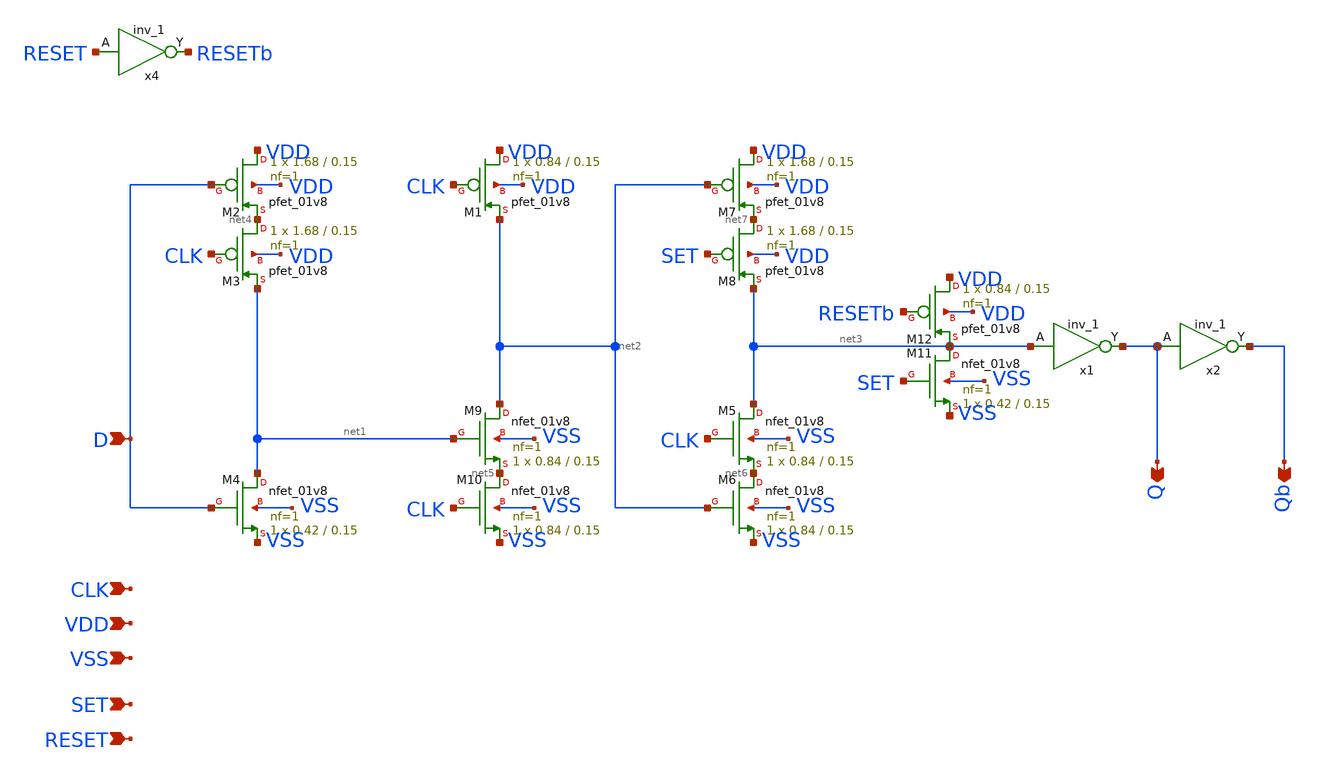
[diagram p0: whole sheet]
** sch_path: module/sample_clk_gen/dff_4.sch
**.subckt dff_4 D Q Qb CLK VDD VSS SET RESET
*.ipin D
*.opin Q
*.opin Qb
*.ipin CLK
*.ipin VDD
*.ipin VSS
*.ipin SET
*.ipin RESET
XM2 VDD D net4 VDD sky130_fd_pr__pfet_01v8 L=0.15 W=1.68 nf=1 ad='int((nf+1)/2) * W/nf * 0.29' as='int((nf+2)/2) * W/nf * 0.29'
+ pd='2*int((nf+1)/2) * (W/nf + 0.29)' ps='2*int((nf+2)/2) * (W/nf + 0.29)' nrd='0.29 / W' nrs='0.29 / W'
+ sa=0 sb=0 sd=0 mult=1 m=1
XM3 net4 CLK net1 VDD sky130_fd_pr__pfet_01v8 L=0.15 W=1.68 nf=1 ad='int((nf+1)/2) * W/nf * 0.29' as='int((nf+2)/2) * W/nf * 0.29'
+ pd='2*int((nf+1)/2) * (W/nf + 0.29)' ps='2*int((nf+2)/2) * (W/nf + 0.29)' nrd='0.29 / W' nrs='0.29 / W'
+ sa=0 sb=0 sd=0 mult=1 m=1
XM9 net2 net1 net5 VSS sky130_fd_pr__nfet_01v8 L=0.15 W=0.84 nf=1 ad='int((nf+1)/2) * W/nf * 0.29' as='int((nf+2)/2) * W/nf * 0.29'
+ pd='2*int((nf+1)/2) * (W/nf + 0.29)' ps='2*int((nf+2)/2) * (W/nf + 0.29)' nrd='0.29 / W' nrs='0.29 / W'
+ sa=0 sb=0 sd=0 mult=1 m=1
XM10 net5 CLK VSS VSS sky130_fd_pr__nfet_01v8 L=0.15 W=0.84 nf=1 ad='int((nf+1)/2) * W/nf * 0.29' as='int((nf+2)/2) * W/nf * 0.29'
+ pd='2*int((nf+1)/2) * (W/nf + 0.29)' ps='2*int((nf+2)/2) * (W/nf + 0.29)' nrd='0.29 / W' nrs='0.29 / W'
+ sa=0 sb=0 sd=0 mult=1 m=1
XM1 VDD CLK net2 VDD sky130_fd_pr__pfet_01v8 L=0.15 W=0.84 nf=1 ad='int((nf+1)/2) * W/nf * 0.29' as='int((nf+2)/2) * W/nf * 0.29'
+ pd='2*int((nf+1)/2) * (W/nf + 0.29)' ps='2*int((nf+2)/2) * (W/nf + 0.29)' nrd='0.29 / W' nrs='0.29 / W'
+ sa=0 sb=0 sd=0 mult=1 m=1
XM4 net1 D VSS VSS sky130_fd_pr__nfet_01v8 L=0.15 W=0.42 nf=1 ad='int((nf+1)/2) * W/nf * 0.29' as='int((nf+2)/2) * W/nf * 0.29'
+ pd='2*int((nf+1)/2) * (W/nf + 0.29)' ps='2*int((nf+2)/2) * (W/nf + 0.29)' nrd='0.29 / W' nrs='0.29 / W'
+ sa=0 sb=0 sd=0 mult=1 m=1
XM5 net3 CLK net6 VSS sky130_fd_pr__nfet_01v8 L=0.15 W=0.84 nf=1 ad='int((nf+1)/2) * W/nf * 0.29' as='int((nf+2)/2) * W/nf * 0.29'
+ pd='2*int((nf+1)/2) * (W/nf + 0.29)' ps='2*int((nf+2)/2) * (W/nf + 0.29)' nrd='0.29 / W' nrs='0.29 / W'
+ sa=0 sb=0 sd=0 mult=1 m=1
XM6 net6 net2 VSS VSS sky130_fd_pr__nfet_01v8 L=0.15 W=0.84 nf=1 ad='int((nf+1)/2) * W/nf * 0.29' as='int((nf+2)/2) * W/nf * 0.29'
+ pd='2*int((nf+1)/2) * (W/nf + 0.29)' ps='2*int((nf+2)/2) * (W/nf + 0.29)' nrd='0.29 / W' nrs='0.29 / W'
+ sa=0 sb=0 sd=0 mult=1 m=1
XM7 VDD net2 net7 VDD sky130_fd_pr__pfet_01v8 L=0.15 W=1.68 nf=1 ad='int((nf+1)/2) * W/nf * 0.29' as='int((nf+2)/2) * W/nf * 0.29'
+ pd='2*int((nf+1)/2) * (W/nf + 0.29)' ps='2*int((nf+2)/2) * (W/nf + 0.29)' nrd='0.29 / W' nrs='0.29 / W'
+ sa=0 sb=0 sd=0 mult=1 m=1
XM8 net7 SET net3 VDD sky130_fd_pr__pfet_01v8 L=0.15 W=1.68 nf=1 ad='int((nf+1)/2) * W/nf * 0.29' as='int((nf+2)/2) * W/nf * 0.29'
+ pd='2*int((nf+1)/2) * (W/nf + 0.29)' ps='2*int((nf+2)/2) * (W/nf + 0.29)' nrd='0.29 / W' nrs='0.29 / W'
+ sa=0 sb=0 sd=0 mult=1 m=1
XM11 net3 SET VSS VSS sky130_fd_pr__nfet_01v8 L=0.15 W=0.42 nf=1 ad='int((nf+1)/2) * W/nf * 0.29' as='int((nf+2)/2) * W/nf * 0.29'
+ pd='2*int((nf+1)/2) * (W/nf + 0.29)' ps='2*int((nf+2)/2) * (W/nf + 0.29)' nrd='0.29 / W' nrs='0.29 / W'
+ sa=0 sb=0 sd=0 mult=1 m=1
XM12 VDD RESETb net3 VDD sky130_fd_pr__pfet_01v8 L=0.15 W=0.84 nf=1 ad='int((nf+1)/2) * W/nf * 0.29'
+ as='int((nf+2)/2) * W/nf * 0.29' pd='2*int((nf+1)/2) * (W/nf + 0.29)' ps='2*int((nf+2)/2) * (W/nf + 0.29)'
+ nrd='0.29 / W' nrs='0.29 / W' sa=0 sb=0 sd=0 mult=1 m=1
x4 RESET VGND VNB VPB VPWR RESETb sky130_fd_sc_hd__inv_1
x1 net3 VGND VNB VPB VPWR Q sky130_fd_sc_hd__inv_1
x2 Q VGND VNB VPB VPWR Qb sky130_fd_sc_hd__inv_1
**.ends
.end
